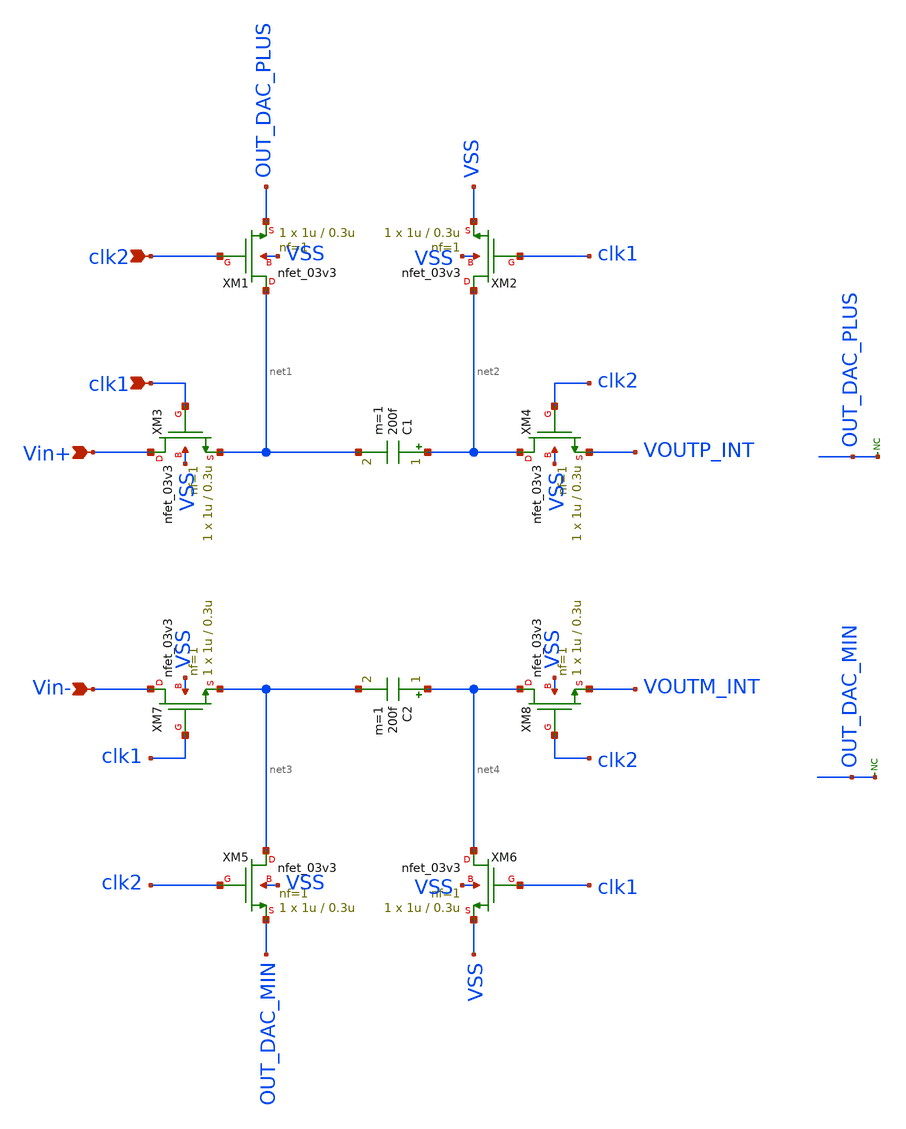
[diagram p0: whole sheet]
** sch_path: src/schematics/integrator_first_order/integrator.sch
**.subckt integrator Vin+ Vin- clk1 clk2
*.ipin Vin+
*.ipin Vin-
*.ipin clk1
*.ipin clk2
XM1 net1 clk2 OUT_DAC_PLUS VSS nfet_03v3 L=0.3u W=1u nf=1 ad='int((nf+1)/2) * W/nf * 0.18u' as='int((nf+2)/2) * W/nf * 0.18u'
+ pd='2*int((nf+1)/2) * (W/nf + 0.18u)' ps='2*int((nf+2)/2) * (W/nf + 0.18u)' nrd='0.18u / W' nrs='0.18u / W'
+ sa=0 sb=0 sd=0 m=1
XM2 net2 clk1 VSS VSS nfet_03v3 L=0.3u W=1u nf=1 ad='int((nf+1)/2) * W/nf * 0.18u' as='int((nf+2)/2) * W/nf * 0.18u'
+ pd='2*int((nf+1)/2) * (W/nf + 0.18u)' ps='2*int((nf+2)/2) * (W/nf + 0.18u)' nrd='0.18u / W' nrs='0.18u / W'
+ sa=0 sb=0 sd=0 m=1
XM3 Vin+ clk1 net1 VSS nfet_03v3 L=0.3u W=1u nf=1 ad='int((nf+1)/2) * W/nf * 0.18u' as='int((nf+2)/2) * W/nf * 0.18u'
+ pd='2*int((nf+1)/2) * (W/nf + 0.18u)' ps='2*int((nf+2)/2) * (W/nf + 0.18u)' nrd='0.18u / W' nrs='0.18u / W'
+ sa=0 sb=0 sd=0 m=1
XM4 net2 clk2 VOUTP_INT VSS nfet_03v3 L=0.3u W=1u nf=1 ad='int((nf+1)/2) * W/nf * 0.18u' as='int((nf+2)/2) * W/nf * 0.18u'
+ pd='2*int((nf+1)/2) * (W/nf + 0.18u)' ps='2*int((nf+2)/2) * (W/nf + 0.18u)' nrd='0.18u / W' nrs='0.18u / W'
+ sa=0 sb=0 sd=0 m=1
C1 net2 net1 200f m=1
XM5 net3 clk2 OUT_DAC_MIN VSS nfet_03v3 L=0.3u W=1u nf=1 ad='int((nf+1)/2) * W/nf * 0.18u' as='int((nf+2)/2) * W/nf * 0.18u'
+ pd='2*int((nf+1)/2) * (W/nf + 0.18u)' ps='2*int((nf+2)/2) * (W/nf + 0.18u)' nrd='0.18u / W' nrs='0.18u / W'
+ sa=0 sb=0 sd=0 m=1
XM6 net4 clk1 VSS VSS nfet_03v3 L=0.3u W=1u nf=1 ad='int((nf+1)/2) * W/nf * 0.18u' as='int((nf+2)/2) * W/nf * 0.18u'
+ pd='2*int((nf+1)/2) * (W/nf + 0.18u)' ps='2*int((nf+2)/2) * (W/nf + 0.18u)' nrd='0.18u / W' nrs='0.18u / W'
+ sa=0 sb=0 sd=0 m=1
XM7 Vin- clk1 net3 VSS nfet_03v3 L=0.3u W=1u nf=1 ad='int((nf+1)/2) * W/nf * 0.18u' as='int((nf+2)/2) * W/nf * 0.18u'
+ pd='2*int((nf+1)/2) * (W/nf + 0.18u)' ps='2*int((nf+2)/2) * (W/nf + 0.18u)' nrd='0.18u / W' nrs='0.18u / W'
+ sa=0 sb=0 sd=0 m=1
XM8 net4 clk2 VOUTM_INT VSS nfet_03v3 L=0.3u W=1u nf=1 ad='int((nf+1)/2) * W/nf * 0.18u' as='int((nf+2)/2) * W/nf * 0.18u'
+ pd='2*int((nf+1)/2) * (W/nf + 0.18u)' ps='2*int((nf+2)/2) * (W/nf + 0.18u)' nrd='0.18u / W' nrs='0.18u / W'
+ sa=0 sb=0 sd=0 m=1
C2 net4 net3 200f m=1
* noconn OUT_DAC_PLUS
* noconn OUT_DAC_MIN
**.ends
.end
